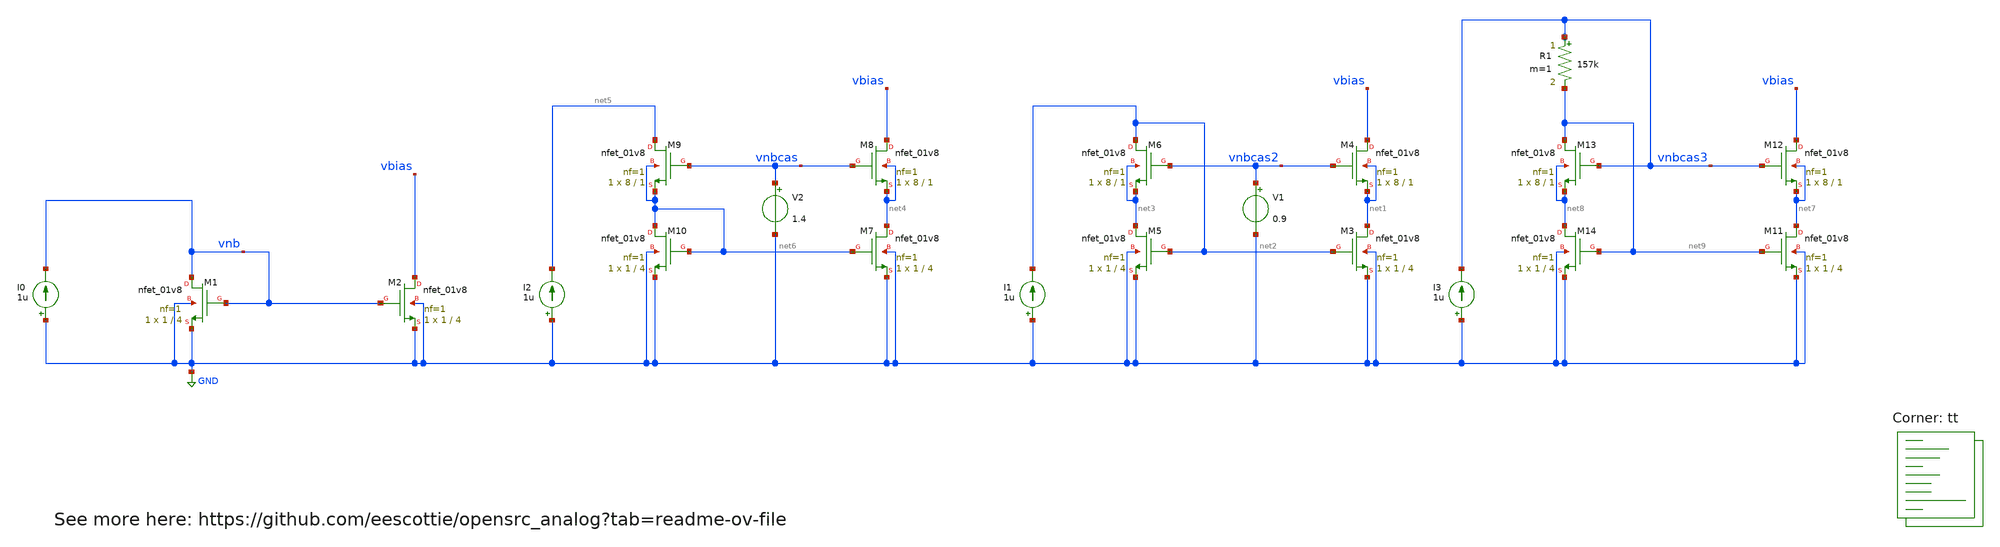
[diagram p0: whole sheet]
** sch_path: current_mirror.sch
**.subckt current_mirror
XM1 vnb vnb GND GND sky130_fd_pr__nfet_01v8 L=4 W=1 nf=1 ad='int((nf+1)/2) * W/nf * 0.29' as='int((nf+2)/2) * W/nf * 0.29'
+ pd='2*int((nf+1)/2) * (W/nf + 0.29)' ps='2*int((nf+2)/2) * (W/nf + 0.29)' nrd='0.29 / W' nrs='0.29 / W'
+ sa=0 sb=0 sd=0 mult=1 m=1
I0 GND vnb 1u
XM2 vbias vnb GND GND sky130_fd_pr__nfet_01v8 L=4 W=1 nf=1 ad='int((nf+1)/2) * W/nf * 0.29' as='int((nf+2)/2) * W/nf * 0.29'
+ pd='2*int((nf+1)/2) * (W/nf + 0.29)' ps='2*int((nf+2)/2) * (W/nf + 0.29)' nrd='0.29 / W' nrs='0.29 / W'
+ sa=0 sb=0 sd=0 mult=1 m=1
XM3 net1 net2 GND GND sky130_fd_pr__nfet_01v8 L=4 W=1 nf=1 ad='int((nf+1)/2) * W/nf * 0.29' as='int((nf+2)/2) * W/nf * 0.29'
+ pd='2*int((nf+1)/2) * (W/nf + 0.29)' ps='2*int((nf+2)/2) * (W/nf + 0.29)' nrd='0.29 / W' nrs='0.29 / W'
+ sa=0 sb=0 sd=0 mult=1 m=1
XM4 vbias vnbcas2 net1 net1 sky130_fd_pr__nfet_01v8 L=1 W=8 nf=1 ad='int((nf+1)/2) * W/nf * 0.29' as='int((nf+2)/2) * W/nf * 0.29'
+ pd='2*int((nf+1)/2) * (W/nf + 0.29)' ps='2*int((nf+2)/2) * (W/nf + 0.29)' nrd='0.29 / W' nrs='0.29 / W'
+ sa=0 sb=0 sd=0 mult=1 m=1
V1 vnbcas2 GND 0.9
I1 GND net2 1u
XM6 net2 vnbcas2 net3 net3 sky130_fd_pr__nfet_01v8 L=1 W=8 nf=1 ad='int((nf+1)/2) * W/nf * 0.29' as='int((nf+2)/2) * W/nf * 0.29'
+ pd='2*int((nf+1)/2) * (W/nf + 0.29)' ps='2*int((nf+2)/2) * (W/nf + 0.29)' nrd='0.29 / W' nrs='0.29 / W'
+ sa=0 sb=0 sd=0 mult=1 m=1
XM5 net3 net2 GND GND sky130_fd_pr__nfet_01v8 L=4 W=1 nf=1 ad='int((nf+1)/2) * W/nf * 0.29' as='int((nf+2)/2) * W/nf * 0.29'
+ pd='2*int((nf+1)/2) * (W/nf + 0.29)' ps='2*int((nf+2)/2) * (W/nf + 0.29)' nrd='0.29 / W' nrs='0.29 / W'
+ sa=0 sb=0 sd=0 mult=1 m=1
XM7 net4 net6 GND GND sky130_fd_pr__nfet_01v8 L=4 W=1 nf=1 ad='int((nf+1)/2) * W/nf * 0.29' as='int((nf+2)/2) * W/nf * 0.29'
+ pd='2*int((nf+1)/2) * (W/nf + 0.29)' ps='2*int((nf+2)/2) * (W/nf + 0.29)' nrd='0.29 / W' nrs='0.29 / W'
+ sa=0 sb=0 sd=0 mult=1 m=1
XM8 vbias vnbcas net4 net4 sky130_fd_pr__nfet_01v8 L=1 W=8 nf=1 ad='int((nf+1)/2) * W/nf * 0.29' as='int((nf+2)/2) * W/nf * 0.29'
+ pd='2*int((nf+1)/2) * (W/nf + 0.29)' ps='2*int((nf+2)/2) * (W/nf + 0.29)' nrd='0.29 / W' nrs='0.29 / W'
+ sa=0 sb=0 sd=0 mult=1 m=1
V2 vnbcas GND 1.4
I2 GND net5 1u
XM9 net5 vnbcas net6 net6 sky130_fd_pr__nfet_01v8 L=1 W=8 nf=1 ad='int((nf+1)/2) * W/nf * 0.29' as='int((nf+2)/2) * W/nf * 0.29'
+ pd='2*int((nf+1)/2) * (W/nf + 0.29)' ps='2*int((nf+2)/2) * (W/nf + 0.29)' nrd='0.29 / W' nrs='0.29 / W'
+ sa=0 sb=0 sd=0 mult=1 m=1
XM10 net6 net6 GND GND sky130_fd_pr__nfet_01v8 L=4 W=1 nf=1 ad='int((nf+1)/2) * W/nf * 0.29' as='int((nf+2)/2) * W/nf * 0.29'
+ pd='2*int((nf+1)/2) * (W/nf + 0.29)' ps='2*int((nf+2)/2) * (W/nf + 0.29)' nrd='0.29 / W' nrs='0.29 / W'
+ sa=0 sb=0 sd=0 mult=1 m=1
XM11 net7 net9 GND GND sky130_fd_pr__nfet_01v8 L=4 W=1 nf=1 ad='int((nf+1)/2) * W/nf * 0.29' as='int((nf+2)/2) * W/nf * 0.29'
+ pd='2*int((nf+1)/2) * (W/nf + 0.29)' ps='2*int((nf+2)/2) * (W/nf + 0.29)' nrd='0.29 / W' nrs='0.29 / W'
+ sa=0 sb=0 sd=0 mult=1 m=1
XM12 vbias vnbcas3 net7 net7 sky130_fd_pr__nfet_01v8 L=1 W=8 nf=1 ad='int((nf+1)/2) * W/nf * 0.29' as='int((nf+2)/2) * W/nf * 0.29'
+ pd='2*int((nf+1)/2) * (W/nf + 0.29)' ps='2*int((nf+2)/2) * (W/nf + 0.29)' nrd='0.29 / W' nrs='0.29 / W'
+ sa=0 sb=0 sd=0 mult=1 m=1
I3 GND vnbcas3 1u
XM13 net9 vnbcas3 net8 net8 sky130_fd_pr__nfet_01v8 L=1 W=8 nf=1 ad='int((nf+1)/2) * W/nf * 0.29' as='int((nf+2)/2) * W/nf * 0.29'
+ pd='2*int((nf+1)/2) * (W/nf + 0.29)' ps='2*int((nf+2)/2) * (W/nf + 0.29)' nrd='0.29 / W' nrs='0.29 / W'
+ sa=0 sb=0 sd=0 mult=1 m=1
XM14 net8 net9 GND GND sky130_fd_pr__nfet_01v8 L=4 W=1 nf=1 ad='int((nf+1)/2) * W/nf * 0.29' as='int((nf+2)/2) * W/nf * 0.29'
+ pd='2*int((nf+1)/2) * (W/nf + 0.29)' ps='2*int((nf+2)/2) * (W/nf + 0.29)' nrd='0.29 / W' nrs='0.29 / W'
+ sa=0 sb=0 sd=0 mult=1 m=1
R1 vnbcas3 net9 157k m=1
**** begin user architecture code


.option savecurrents
vb vbias 0 0.9
.save all
.control
*dc I0 0 1u 10n
dc vb 0 1.8 10m
remzerovec
*save @m.xm1.msky130_fd_pr__nfet_01v8[gm]
*save @m.xm1.msky130_fd_pr__nfet_01v8[vth]
*save @m.xm1.msky130_fd_pr__nfet_01v8[gds]
*save @m.xm1.msky130_fd_pr__nfet_01v8[vdsat]

set filetype=binary
write current_mirror.raw
set appendwrite
op
show m : vgs : vth : vds : vdsat : gm : gds

* The followign are obsolete with the show statement above
* print @m.xm1.msky130_fd_pr__nfet_01v8[gm]
* print @m.xm1.msky130_fd_pr__nfet_01v8[gds]
* print @m.xm1.msky130_fd_pr__nfet_01v8[vdsat]
* print @m.xm1.msky130_fd_pr__nfet_01v8[vth]

write current_mirror.raw
.endc


.lib $::SKYWATER_MODELS/sky130.lib.spice tt
**** end user architecture code
**.ends
.GLOBAL GND
.end
